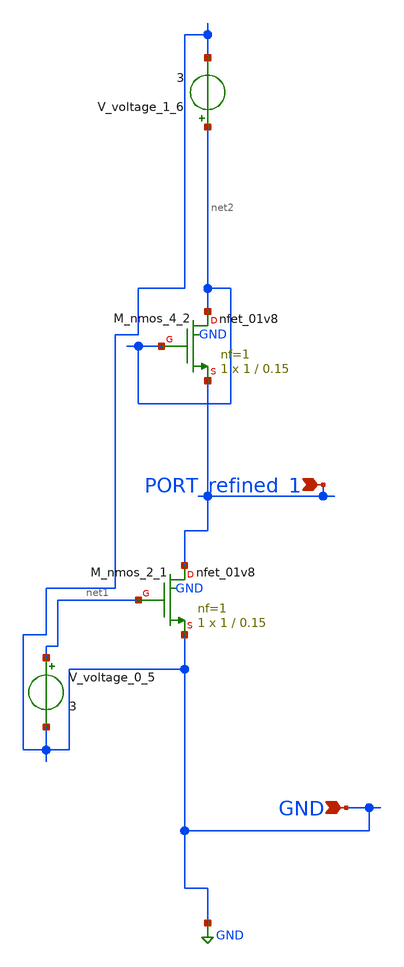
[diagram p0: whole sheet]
** sch_path: schematics/SchemGen/10_1007_s12274-008-8033-4_09_002.sch
**.subckt 10_1007_s12274-008-8033-4_09_002 PORT_refined_1 GND
*.ipin PORT_refined_1
*.ipin GND
XM_nmos_2_1 PORT_refined_1 net1 GND GND sky130_fd_pr__nfet_01v8 L=0.15 W=1 nf=1 ad='int((1 + 1)/2) * 1 / 1 * 0.29'
+ as='int((1 + 2)/2) * 1 / 1 * 0.29' pd='2*int((1 + 1)/2) * (1 / 1 + 0.29)' ps='2*int((1 + 2)/2) * (1 / 1 + 0.29)'
+ nrd='0.29 / 1 ' nrs='0.29 / 1 ' sa=0 sb=0 sd=0 mult=1 m=1
XM_nmos_4_2 net2 net2 PORT_refined_1 GND sky130_fd_pr__nfet_01v8 L=0.15 W=1 nf=1 ad='int((1 + 1)/2) * 1 / 1 * 0.29'
+ as='int((1 + 2)/2) * 1 / 1 * 0.29' pd='2*int((1 + 1)/2) * (1 / 1 + 0.29)' ps='2*int((1 + 2)/2) * (1 / 1 + 0.29)'
+ nrd='0.29 / 1 ' nrs='0.29 / 1 ' sa=0 sb=0 sd=0 mult=1 m=1
V_voltage_0_5 net1 GND 3
V_voltage_1_6 net2 GND 3
**.ends
.GLOBAL GND
.end
